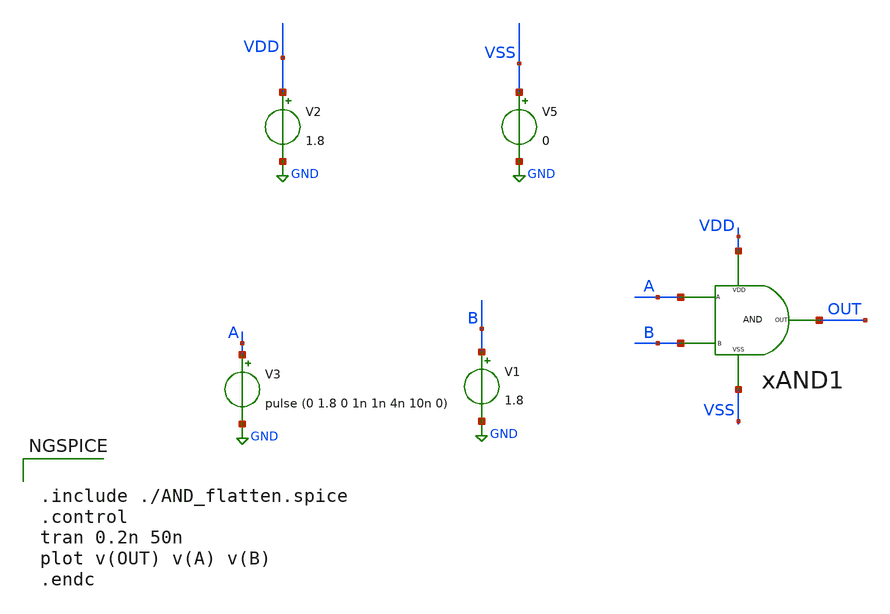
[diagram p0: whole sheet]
** sch_path: xschem/DC_DC_Converter_xschem/DC_DC_Converter/Delay_block_revised/AND_GATE/AND_PEX_TB.sch
**.subckt AND_PEX_TB
V2 VDD GND 1.8
V5 VSS GND 0
V1 B GND 1.8
V3 A GND pulse (0 1.8 0 1n 1n 4n 10n 0)
xAND1 VDD VSS A B OUT AND_PEX
**** begin user architecture code


.include ./AND_flatten.spice
.control
tran 0.2n 50n
plot v(OUT) v(A) v(B)
.endc


** manual skywater pdks install (with patches applied)
* .lib $::SKYWATER_MODELS/models/sky130.lib.spice tt

** opencircuitdesign pdks install
.lib $::SKYWATER_MODELS/sky130.lib.spice tt
.include $::SKYWATER_STDCELLS/sky130_fd_sc_hd.spice

**** end user architecture code
**.ends
.GLOBAL GND
.end
